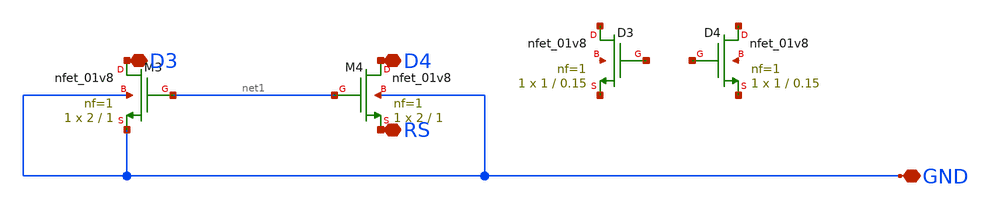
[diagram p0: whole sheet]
** sch_path: opamp/mag/nmoscs/nmos.sch
**.subckt nmos GND RS D4 D3
*.iopin GND
*.iopin RS
*.iopin D4
*.iopin D3
XM3 D3 net1 GND GND sky130_fd_pr__nfet_01v8 L=1 W=2 nf=1 ad='int((nf+1)/2) * W/nf * 0.29' as='int((nf+2)/2) * W/nf * 0.29'
+ pd='2*int((nf+1)/2) * (W/nf + 0.29)' ps='2*int((nf+2)/2) * (W/nf + 0.29)' nrd='0.29 / W' nrs='0.29 / W'
+ sa=0 sb=0 sd=0 mult=1 m=1
XM4 D4 net1 RS GND sky130_fd_pr__nfet_01v8 L=1 W=2 nf=1 ad='int((nf+1)/2) * W/nf * 0.29' as='int((nf+2)/2) * W/nf * 0.29'
+ pd='2*int((nf+1)/2) * (W/nf + 0.29)' ps='2*int((nf+2)/2) * (W/nf + 0.29)' nrd='0.29 / W' nrs='0.29 / W'
+ sa=0 sb=0 sd=0 mult=1 m=1
XD4 net2 net3 net4 net5 sky130_fd_pr__nfet_01v8 L=0.15 W=1 nf=1 ad='int((nf+1)/2) * W/nf * 0.29' as='int((nf+2)/2) * W/nf * 0.29'
+ pd='2*int((nf+1)/2) * (W/nf + 0.29)' ps='2*int((nf+2)/2) * (W/nf + 0.29)' nrd='0.29 / W' nrs='0.29 / W'
+ sa=0 sb=0 sd=0 mult=1 m=1
XD3 net6 net7 net8 net9 sky130_fd_pr__nfet_01v8 L=0.15 W=1 nf=1 ad='int((nf+1)/2) * W/nf * 0.29' as='int((nf+2)/2) * W/nf * 0.29'
+ pd='2*int((nf+1)/2) * (W/nf + 0.29)' ps='2*int((nf+2)/2) * (W/nf + 0.29)' nrd='0.29 / W' nrs='0.29 / W'
+ sa=0 sb=0 sd=0 mult=1 m=1
**.ends
.end
